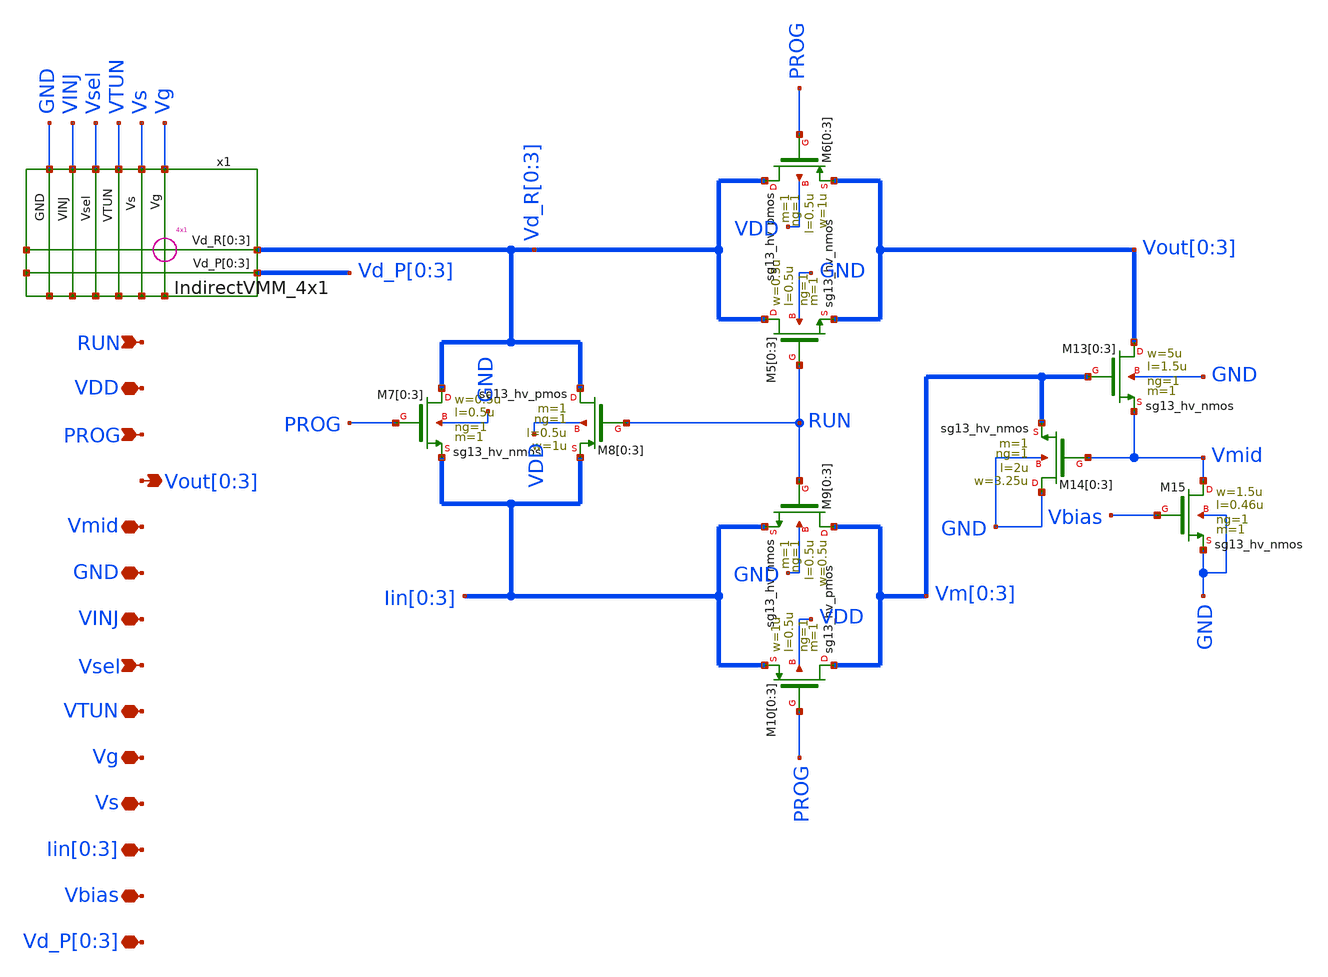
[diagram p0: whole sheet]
** sch_path: ihp130_cells/4WTA_Indirect/4WTA_Indirect.sch
**.subckt 4WTA_Indirect RUN VDD PROG Vout[0],Vout[1],Vout[2],Vout[3] Vmid GND VINJ Vsel VTUN Vg Vs
*+ Iin[0],Iin[1],Iin[2],Iin[3] Vbias Vd_P[0],Vd_P[1],Vd_P[2],Vd_P[3]
*.ipin RUN
*.iopin VDD
*.ipin PROG
*.opin Vout[0],Vout[1],Vout[2],Vout[3]
*.iopin Vmid
*.iopin GND
*.iopin VINJ
*.ipin Vsel
*.iopin VTUN
*.iopin Vg
*.iopin Vs
*.iopin Iin[0],Iin[1],Iin[2],Iin[3]
*.iopin Vbias
*.iopin Vd_P[0],Vd_P[1],Vd_P[2],Vd_P[3]
XM5[0] Vd_R[0] RUN Vout[0] GND sg13_hv_nmos w=0.5u l=0.5u ng=1 m=1 mm_ok=1
XM5[1] Vd_R[1] RUN Vout[1] GND sg13_hv_nmos w=0.5u l=0.5u ng=1 m=1 mm_ok=1
XM5[2] Vd_R[2] RUN Vout[2] GND sg13_hv_nmos w=0.5u l=0.5u ng=1 m=1 mm_ok=1
XM5[3] Vd_R[3] RUN Vout[3] GND sg13_hv_nmos w=0.5u l=0.5u ng=1 m=1 mm_ok=1
XM6[0] Vd_R[0] PROG Vout[0] VDD sg13_hv_pmos w=1u l=0.5u ng=1 m=1 mm_ok=1
XM6[1] Vd_R[1] PROG Vout[1] VDD sg13_hv_pmos w=1u l=0.5u ng=1 m=1 mm_ok=1
XM6[2] Vd_R[2] PROG Vout[2] VDD sg13_hv_pmos w=1u l=0.5u ng=1 m=1 mm_ok=1
XM6[3] Vd_R[3] PROG Vout[3] VDD sg13_hv_pmos w=1u l=0.5u ng=1 m=1 mm_ok=1
XM7[0] Vd_R[0] PROG Iin[0] GND sg13_hv_nmos w=0.5u l=0.5u ng=1 m=1 mm_ok=1
XM7[1] Vd_R[1] PROG Iin[1] GND sg13_hv_nmos w=0.5u l=0.5u ng=1 m=1 mm_ok=1
XM7[2] Vd_R[2] PROG Iin[2] GND sg13_hv_nmos w=0.5u l=0.5u ng=1 m=1 mm_ok=1
XM7[3] Vd_R[3] PROG Iin[3] GND sg13_hv_nmos w=0.5u l=0.5u ng=1 m=1 mm_ok=1
XM8[0] Vd_R[0] RUN Iin[0] VDD sg13_hv_pmos w=1u l=0.5u ng=1 m=1 mm_ok=1
XM8[1] Vd_R[1] RUN Iin[1] VDD sg13_hv_pmos w=1u l=0.5u ng=1 m=1 mm_ok=1
XM8[2] Vd_R[2] RUN Iin[2] VDD sg13_hv_pmos w=1u l=0.5u ng=1 m=1 mm_ok=1
XM8[3] Vd_R[3] RUN Iin[3] VDD sg13_hv_pmos w=1u l=0.5u ng=1 m=1 mm_ok=1
XM9[0] Vm[0] RUN Iin[0] GND sg13_hv_nmos w=0.5u l=0.5u ng=1 m=1 mm_ok=1
XM9[1] Vm[1] RUN Iin[1] GND sg13_hv_nmos w=0.5u l=0.5u ng=1 m=1 mm_ok=1
XM9[2] Vm[2] RUN Iin[2] GND sg13_hv_nmos w=0.5u l=0.5u ng=1 m=1 mm_ok=1
XM9[3] Vm[3] RUN Iin[3] GND sg13_hv_nmos w=0.5u l=0.5u ng=1 m=1 mm_ok=1
XM10[0] Vm[0] PROG Iin[0] VDD sg13_hv_pmos w=1u l=0.5u ng=1 m=1 mm_ok=1
XM10[1] Vm[1] PROG Iin[1] VDD sg13_hv_pmos w=1u l=0.5u ng=1 m=1 mm_ok=1
XM10[2] Vm[2] PROG Iin[2] VDD sg13_hv_pmos w=1u l=0.5u ng=1 m=1 mm_ok=1
XM10[3] Vm[3] PROG Iin[3] VDD sg13_hv_pmos w=1u l=0.5u ng=1 m=1 mm_ok=1
XM13[0] Vout[0] Vm[0] Vmid GND sg13_hv_nmos w=5u l=1.5u ng=1 m=1 mm_ok=1
XM13[1] Vout[1] Vm[1] Vmid GND sg13_hv_nmos w=5u l=1.5u ng=1 m=1 mm_ok=1
XM13[2] Vout[2] Vm[2] Vmid GND sg13_hv_nmos w=5u l=1.5u ng=1 m=1 mm_ok=1
XM13[3] Vout[3] Vm[3] Vmid GND sg13_hv_nmos w=5u l=1.5u ng=1 m=1 mm_ok=1
XM14[0] GND Vmid Vm[0] GND sg13_hv_nmos w=3.25u l=2u ng=1 m=1 mm_ok=1
XM14[1] GND Vmid Vm[1] GND sg13_hv_nmos w=3.25u l=2u ng=1 m=1 mm_ok=1
XM14[2] GND Vmid Vm[2] GND sg13_hv_nmos w=3.25u l=2u ng=1 m=1 mm_ok=1
XM14[3] GND Vmid Vm[3] GND sg13_hv_nmos w=3.25u l=2u ng=1 m=1 mm_ok=1
XM15 Vmid Vbias GND GND sg13_hv_nmos w=1.5u l=0.46u ng=1 m=1 mm_ok=1
x1 Vd_P[0] Vd_P[1] Vd_P[2] Vd_P[3] Vd_R[0] Vd_R[1] Vd_R[2] Vd_R[3] Vg Vs VTUN Vsel VINJ GND net1
+ IndirectVMM_4x1
**.ends
.end
